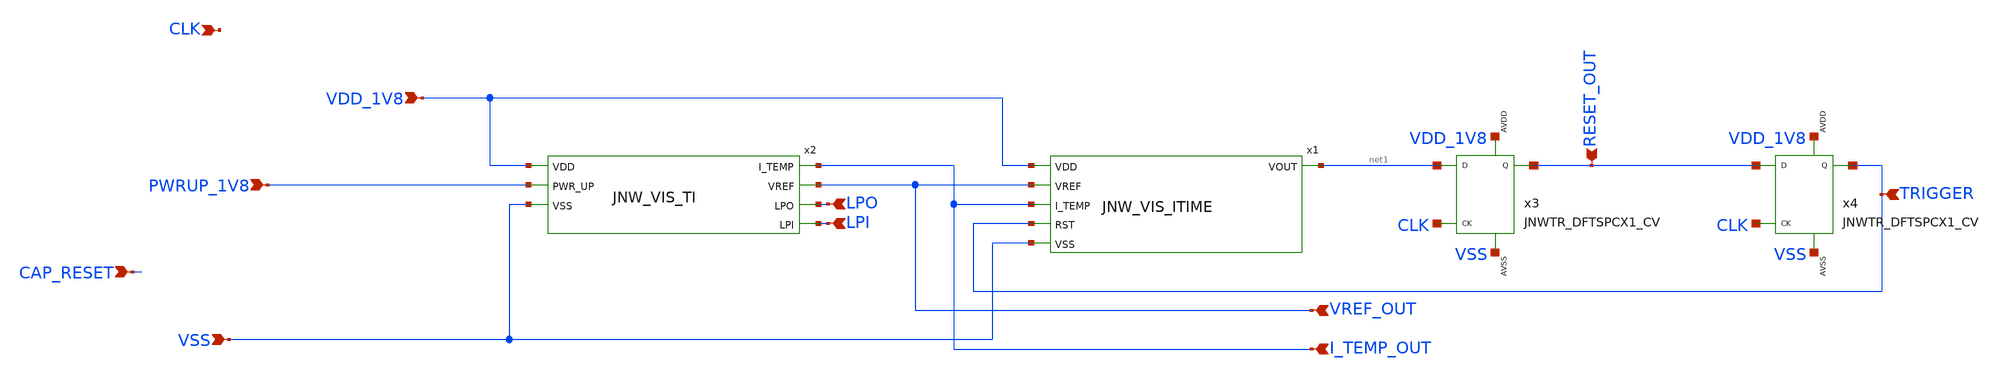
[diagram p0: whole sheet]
** sch_path: design/JNW_GR02_SKY130A/JNW_GR02.sch
**.subckt JNW_GR02 VDD_1V8 VSS PWRUP_1V8 TRIGGER CAP_RESET I_TEMP_OUT LPI LPO VREF_OUT CLK RESET_OUT
*.ipin VDD_1V8
*.ipin VSS
*.ipin PWRUP_1V8
*.ipin TRIGGER
*.ipin CAP_RESET
*.ipin I_TEMP_OUT
*.ipin LPI
*.ipin LPO
*.ipin VREF_OUT
*.ipin CLK
*.ipin RESET_OUT
x1 VDD_1V8 VREF_OUT net1 I_TEMP_OUT TRIGGER VSS JNW_VIS_ITIME
x2 I_TEMP_OUT VDD_1V8 VREF_OUT LPO LPI PWRUP_1V8 VSS JNW_VIS_TI
x3 net1 CLK RESET_OUT VDD_1V8 VSS JNWTR_DFTSPCX1_CV xoffset=0 yoffset=0 angle=0
x4 RESET_OUT CLK TRIGGER VDD_1V8 VSS JNWTR_DFTSPCX1_CV xoffset=0 yoffset=0 angle=0
**.ends
.end
